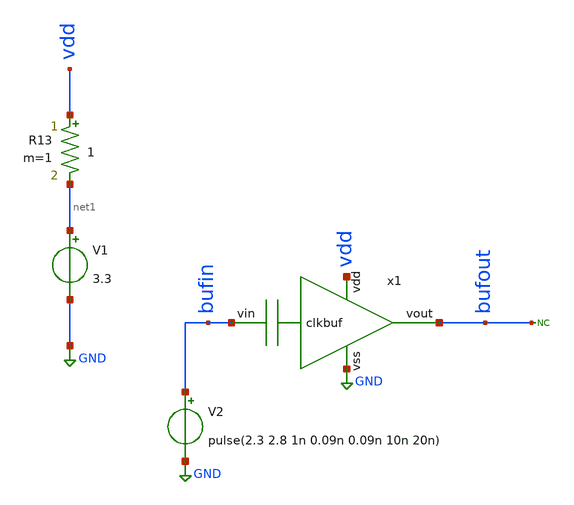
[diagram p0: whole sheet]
** sch_path: xschem/tb_clkbuf.sch
**.subckt tb_clkbuf
x1 vdd bufin bufout GND clkbuf
* noconn bufout
V1 net1 GND 3.3
V2 bufin GND pulse(2.3 2.8 1n 0.09n 0.09n 10n 20n)
R13 vdd net1 1 m=1
**** begin user architecture code


.include /usr/local/share/pdk/gf180mcuD/libs.tech/ngspice/design.ngspice
.lib /usr/local/share/pdk/gf180mcuD/libs.tech/ngspice/sm141064.ngspice ss
.lib /usr/local/share/pdk/gf180mcuD/libs.tech/ngspice/sm141064.ngspice cap_mim
.lib /usr/local/share/pdk/gf180mcuD/libs.tech/ngspice/sm141064.ngspice mimcap_ff
.lib /usr/local/share/pdk/gf180mcuD/libs.tech/ngspice/sm141064.ngspice moscap_typical
.lib /usr/local/share/pdk/gf180mcuD/libs.tech/ngspice/sm141064.ngspice res_typical
.option temp=110

.control
save all

tran 12p 50n
plot bufin bufout
plot i(V1) avg(i(V1))

.endc


**** end user architecture code
**.ends
.GLOBAL GND
.end
